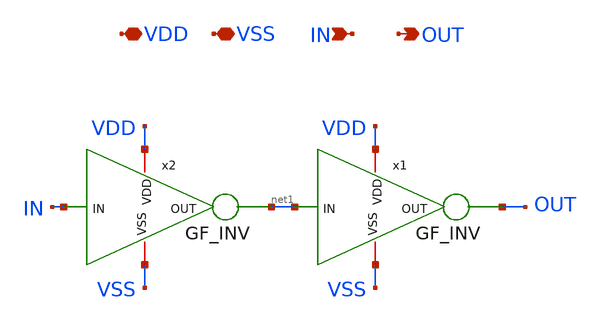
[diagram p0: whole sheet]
** sch_path: Clock_Generator_PAKISTAN_02/Schematics/buffer.sch
**.subckt buffer VDD VSS IN OUT
*.iopin VDD
*.iopin VSS
*.ipin IN
*.opin OUT
x1 VSS VDD OUT net1 GF_INV
x2 VSS VDD net1 IN GF_INV
**.ends

* expanding   symbol:  GF_INV.sym # of pins=4
** sym_path: GF_INV.sym
** sch_path: GF_INV.sch
.subckt GF_INV VSS VDD OUT IN
*.iopin VDD
*.iopin VSS
*.ipin IN
*.opin OUT
XM1 OUT IN VSS VSS nfet_03v3 L=0.56u W=0.56u nf=1 ad='int((nf+1)/2) * W/nf * 0.18u' as='int((nf+2)/2) * W/nf * 0.18u'
+ pd='2*int((nf+1)/2) * (W/nf + 0.18u)' ps='2*int((nf+2)/2) * (W/nf + 0.18u)' nrd='0.18u / W' nrs='0.18u / W'
+ sa=0 sb=0 sd=0 m=1
XM2 OUT IN VDD VDD pfet_03v3 L=0.56u W=1.12u nf=1 ad='int((nf+1)/2) * W/nf * 0.18u' as='int((nf+2)/2) * W/nf * 0.18u'
+ pd='2*int((nf+1)/2) * (W/nf + 0.18u)' ps='2*int((nf+2)/2) * (W/nf + 0.18u)' nrd='0.18u / W' nrs='0.18u / W'
+ sa=0 sb=0 sd=0 m=1
.ends

.end
